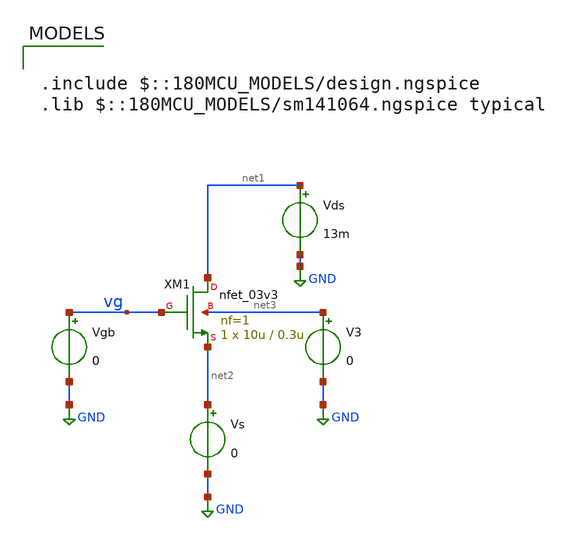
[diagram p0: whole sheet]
** sch_path: legacy/Examples/GF180MCU/xschem/Extraction/nmos_ext.sch
**.subckt nmos_ext
Vds net1 GND 13m
V3 net3 GND 0
Vs net2 GND 0
XM1 net1 vg net2 net3 nfet_03v3 L=0.3u W=10u nf=1 ad='int((nf+1)/2) * W/nf * 0.18u' as='int((nf+2)/2) * W/nf * 0.18u'
+ pd='2*int((nf+1)/2) * (W/nf + 0.18u)' ps='2*int((nf+2)/2) * (W/nf + 0.18u)' nrd='0.18u / W' nrs='0.18u / W'
+ sa=0 sb=0 sd=0 m=1
Vgb vg GND 0
**** begin user architecture code

.include $::180MCU_MODELS/design.ngspice
.lib $::180MCU_MODELS/sm141064.ngspice typical




.control
save all
dc Vgb 0.05 3.3 1m

let gm_id = deriv(ln(i(Vs)))
save gm_id

meas dc gm_id_max MAX gm_id
let gm_id_vt = 0.531*gm_id_max
save gm_id_vt

meas dc vt0 FIND V(vg) WHEN gm_id=gm_id_vt
meas dc is_ FIND i(Vs) WHEN V(vg)=vt0

let is = is_/0.88
let VT_val=0.026
let n = 1/(gm_id_max*VT_val)
save is vt0 n
echo
echo
echo

echo Extracted parameters:
print is vt0 n


echo
echo
echo

remzerovec
write nmos_ext.raw

.endc



**** end user architecture code
**.ends
.GLOBAL GND
.end
